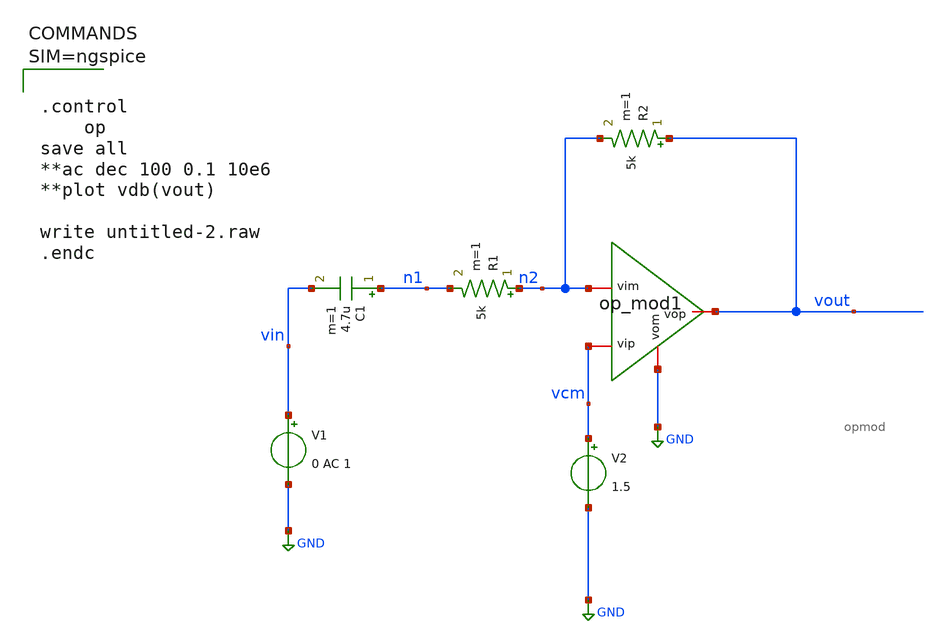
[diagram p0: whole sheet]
** sch_path: untitled-2.sch
**.subckt untitled-2
C1 n1 vin 4.7u m=1
R1 n2 n1 5k m=1
R2 vout n2 5k m=1
V1 vin GND 0 AC 1
V2 vcm GND 1.5
x1 vout vcm n2 GND opmod
**** begin user architecture code



.control
	op
save all
**ac dec 100 0.1 10e6
**plot vdb(vout)

write untitled-2.raw
.endc



**** end user architecture code
**.ends

* expanding   symbol:  opmod.sym # of pins=4
** sym_path: opmod.sym
** sch_path: opmod.sch
.subckt opmod vop vip vim vom
*.iopin vop
*.iopin vom
*.iopin vim
*.iopin vip
E1 vop vom vip vim 1000
.ends

.GLOBAL GND
.end
